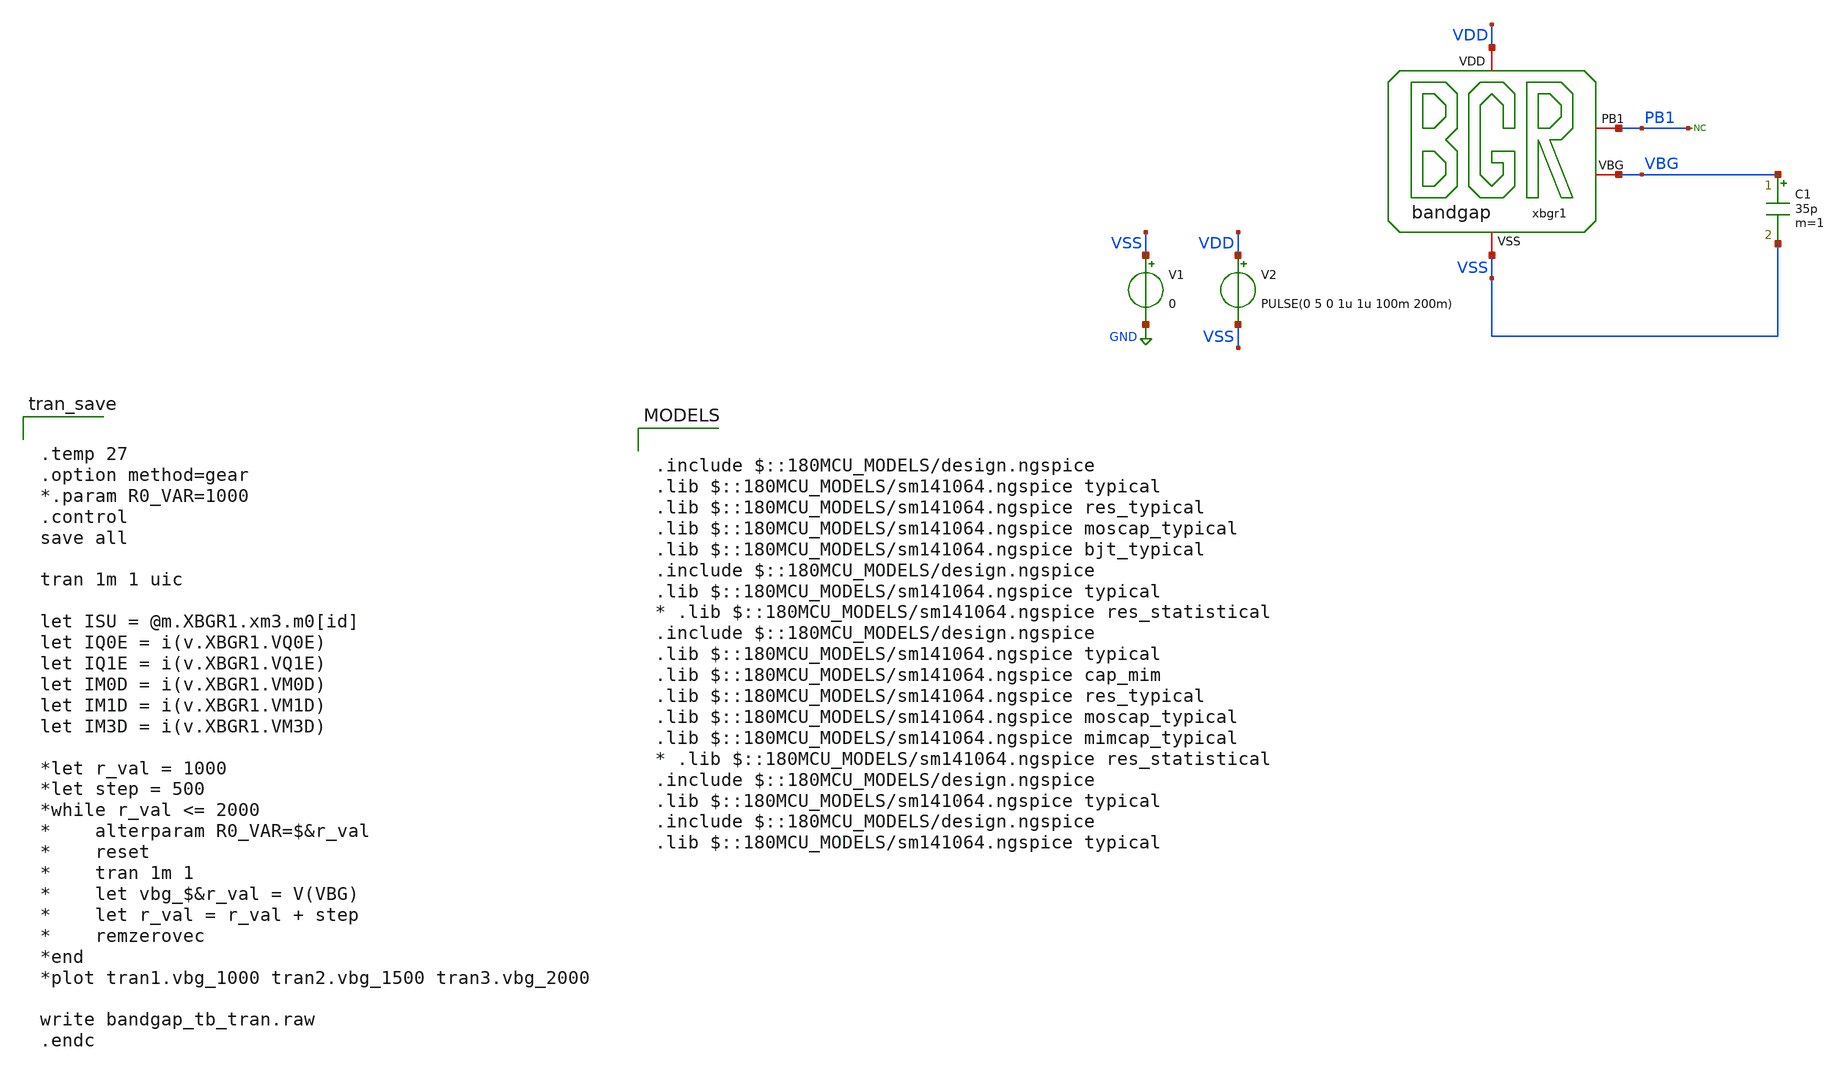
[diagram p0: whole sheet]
** sch_path: bandgap/xschem/sim/bandgap_tb_tran.sch
**.subckt bandgap_tb_tran
V1 VSS GND 0
V2 VDD VSS PULSE(0 5 0 1u 1u 100m 200m)
xbgr1 VDD PB1 VBG VSS bandgap
* noconn PB1
C1 VBG VSS 35p m=1
**** begin user architecture code


.temp 27
.option method=gear
*.param R0_VAR=1000
.control
save all

tran 1m 1 uic

let ISU = @m.XBGR1.xm3.m0[id]
let IQ0E = i(v.XBGR1.VQ0E)
let IQ1E = i(v.XBGR1.VQ1E)
let IM0D = i(v.XBGR1.VM0D)
let IM1D = i(v.XBGR1.VM1D)
let IM3D = i(v.XBGR1.VM3D)

*let r_val = 1000
*let step = 500
*while r_val <= 2000
*	alterparam R0_VAR=$&r_val
*	reset
*	tran 1m 1
*	let vbg_$&r_val = V(VBG)
*	let r_val = r_val + step
*	remzerovec
*end
*plot tran1.vbg_1000 tran2.vbg_1500 tran3.vbg_2000

write bandgap_tb_tran.raw
.endc



.include $::180MCU_MODELS/design.ngspice
.lib $::180MCU_MODELS/sm141064.ngspice typical
.lib $::180MCU_MODELS/sm141064.ngspice res_typical
.lib $::180MCU_MODELS/sm141064.ngspice moscap_typical
.lib $::180MCU_MODELS/sm141064.ngspice bjt_typical
.include $::180MCU_MODELS/design.ngspice
.lib $::180MCU_MODELS/sm141064.ngspice typical
* .lib $::180MCU_MODELS/sm141064.ngspice res_statistical
.include $::180MCU_MODELS/design.ngspice
.lib $::180MCU_MODELS/sm141064.ngspice typical
.lib $::180MCU_MODELS/sm141064.ngspice cap_mim
.lib $::180MCU_MODELS/sm141064.ngspice res_typical
.lib $::180MCU_MODELS/sm141064.ngspice moscap_typical
.lib $::180MCU_MODELS/sm141064.ngspice mimcap_typical
* .lib $::180MCU_MODELS/sm141064.ngspice res_statistical
.include $::180MCU_MODELS/design.ngspice
.lib $::180MCU_MODELS/sm141064.ngspice typical
.include $::180MCU_MODELS/design.ngspice
.lib $::180MCU_MODELS/sm141064.ngspice typical

**** end user architecture code
**.ends

* expanding   symbol:  bandgap/xschem/dev/bandgap.sym # of pins=4
** sym_path: bandgap/cace/testbenches/bandgap.sym
** sch_path: bandgap/cace/testbenches/bandgap.sch
.subckt bandgap VDD PB1 VBG VSS
*.iopin VSS
*.iopin VDD
*.iopin PB1
*.iopin VBG
R0 net7 VSET 1.7k m=1
R1 VSET VSS 7.6k m=1
R2 VB0 VBG 17000 m=1
XQ1 PB1 net8 net6 VSS npn_10p00x10p00 m=12
XQ0 VB0 VB0 net3 VSS npn_10p00x10p00 m=1
XM4 VSS net2 VSS VSS nfet_03v3 L=1u W=19u nf=1 ad='int((nf+1)/2) * W/nf * 0.18u' as='int((nf+2)/2) * W/nf * 0.18u'
+ pd='2*int((nf+1)/2) * (W/nf + 0.18u)' ps='2*int((nf+2)/2) * (W/nf + 0.18u)' nrd='0.18u / W' nrs='0.18u / W'
+ sa=0 sb=0 sd=0 m=1
XM2 net2 VSS VDD VDD pfet_03v3 L=10u W=1u nf=1 ad='int((nf+1)/2) * W/nf * 0.18u' as='int((nf+2)/2) * W/nf * 0.18u'
+ pd='2*int((nf+1)/2) * (W/nf + 0.18u)' ps='2*int((nf+2)/2) * (W/nf + 0.18u)' nrd='0.18u / W' nrs='0.18u / W'
+ sa=0 sb=0 sd=0 m=1
XM3 net5 net2 VDD VDD pfet_03v3 L=2u W=2u nf=1 ad='int((nf+1)/2) * W/nf * 0.18u' as='int((nf+2)/2) * W/nf * 0.18u'
+ pd='2*int((nf+1)/2) * (W/nf + 0.18u)' ps='2*int((nf+2)/2) * (W/nf + 0.18u)' nrd='0.18u / W' nrs='0.18u / W'
+ sa=0 sb=0 sd=0 m=1
XM1 net1 net1 VDD VDD pfet_03v3 L=7.4u W=20u nf=1 ad='int((nf+1)/2) * W/nf * 0.18u' as='int((nf+2)/2) * W/nf * 0.18u'
+ pd='2*int((nf+1)/2) * (W/nf + 0.18u)' ps='2*int((nf+2)/2) * (W/nf + 0.18u)' nrd='0.18u / W' nrs='0.18u / W'
+ sa=0 sb=0 sd=0 m=1
XM0 net4 net1 VDD VDD pfet_03v3 L=7.4u W=20u nf=1 ad='int((nf+1)/2) * W/nf * 0.18u' as='int((nf+2)/2) * W/nf * 0.18u'
+ pd='2*int((nf+1)/2) * (W/nf + 0.18u)' ps='2*int((nf+2)/2) * (W/nf + 0.18u)' nrd='0.18u / W' nrs='0.18u / W'
+ sa=0 sb=0 sd=0 m=1
VQ0E net3 VSET 0
VM0D net4 VB0 0
VM3D net5 VB0 0
VQ1E net6 net7 0
VM1D net1 PB1 0
VQ1B VBG net8 0
.ends

.GLOBAL GND
.end
